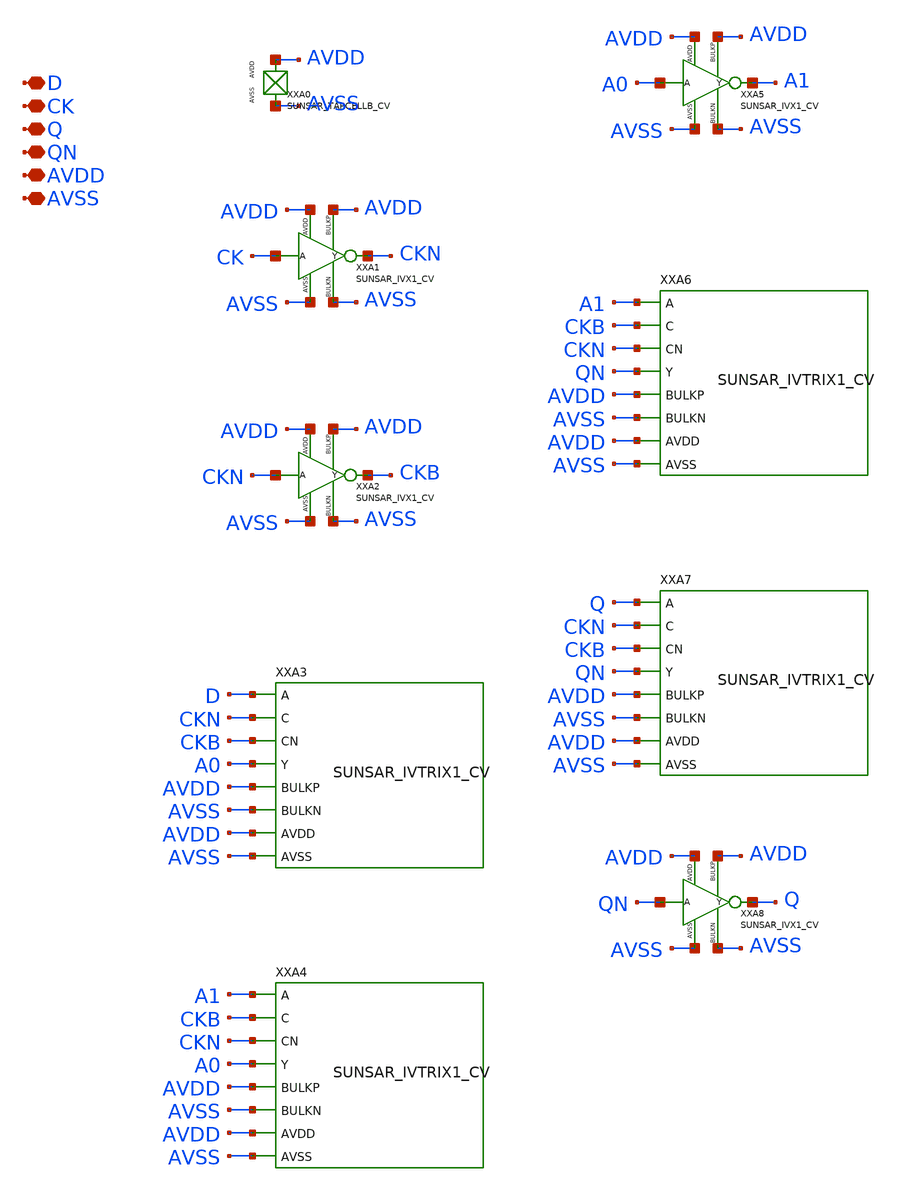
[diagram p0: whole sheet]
** sch_path: design/SUN_SAR9B_SKY130NM/SUNSAR_DFQNX1_CV.sch
**.subckt SUNSAR_DFQNX1_CV D CK Q QN AVDD AVSS
*.iopin D
*.iopin CK
*.iopin Q
*.iopin QN
*.iopin AVDD
*.iopin AVSS
XXA0 AVDD AVSS SUNSAR_TAPCELLB_CV
XXA1 CK CKN AVDD AVSS AVDD AVSS SUNSAR_IVX1_CV
XXA2 CKN CKB AVDD AVSS AVDD AVSS SUNSAR_IVX1_CV
XXA3 D CKN CKB A0 AVDD AVSS AVDD AVSS SUNSAR_IVTRIX1_CV
XXA4 A1 CKB CKN A0 AVDD AVSS AVDD AVSS SUNSAR_IVTRIX1_CV
XXA5 A0 A1 AVDD AVSS AVDD AVSS SUNSAR_IVX1_CV
XXA6 A1 CKB CKN QN AVDD AVSS AVDD AVSS SUNSAR_IVTRIX1_CV
XXA7 Q CKN CKB QN AVDD AVSS AVDD AVSS SUNSAR_IVTRIX1_CV
XXA8 QN Q AVDD AVSS AVDD AVSS SUNSAR_IVX1_CV
**.ends
.end
